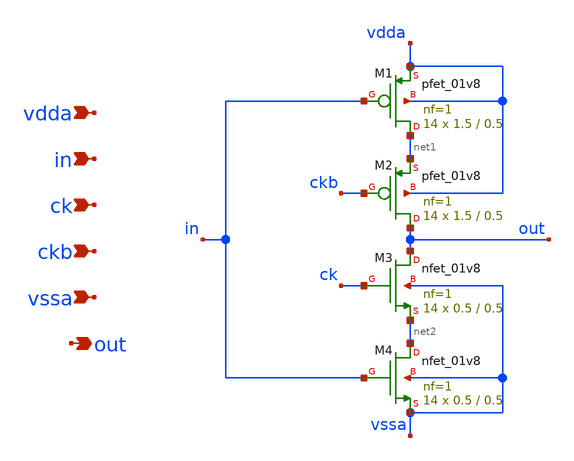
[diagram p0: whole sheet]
** sch_path: xschem/dac_sw_4.sch
**.subckt dac_sw_4 vdda in ck ckb vssa out
*.ipin vdda
*.ipin in
*.ipin ck
*.ipin ckb
*.ipin vssa
*.opin out
XM1 net1 in vdda vdda sky130_fd_pr__pfet_01v8 L=0.5 W=1.5 nf=1 ad='int((nf+1)/2) * W/nf * 0.29' as='int((nf+2)/2) * W/nf * 0.29'
+ pd='2*int((nf+1)/2) * (W/nf + 0.29)' ps='2*int((nf+2)/2) * (W/nf + 0.29)' nrd='0.29 / W' nrs='0.29 / W'
+ sa=0 sb=0 sd=0 mult=14 m=14
XM2 out ckb net1 vdda sky130_fd_pr__pfet_01v8 L=0.5 W=1.5 nf=1 ad='int((nf+1)/2) * W/nf * 0.29' as='int((nf+2)/2) * W/nf * 0.29'
+ pd='2*int((nf+1)/2) * (W/nf + 0.29)' ps='2*int((nf+2)/2) * (W/nf + 0.29)' nrd='0.29 / W' nrs='0.29 / W'
+ sa=0 sb=0 sd=0 mult=14 m=14
XM3 out ck net2 vssa sky130_fd_pr__nfet_01v8 L=0.5 W=0.5 nf=1 ad='int((nf+1)/2) * W/nf * 0.29' as='int((nf+2)/2) * W/nf * 0.29'
+ pd='2*int((nf+1)/2) * (W/nf + 0.29)' ps='2*int((nf+2)/2) * (W/nf + 0.29)' nrd='0.29 / W' nrs='0.29 / W'
+ sa=0 sb=0 sd=0 mult=14 m=14
XM4 net2 in vssa vssa sky130_fd_pr__nfet_01v8 L=0.5 W=0.5 nf=1 ad='int((nf+1)/2) * W/nf * 0.29' as='int((nf+2)/2) * W/nf * 0.29'
+ pd='2*int((nf+1)/2) * (W/nf + 0.29)' ps='2*int((nf+2)/2) * (W/nf + 0.29)' nrd='0.29 / W' nrs='0.29 / W'
+ sa=0 sb=0 sd=0 mult=14 m=14
**.ends
.end
